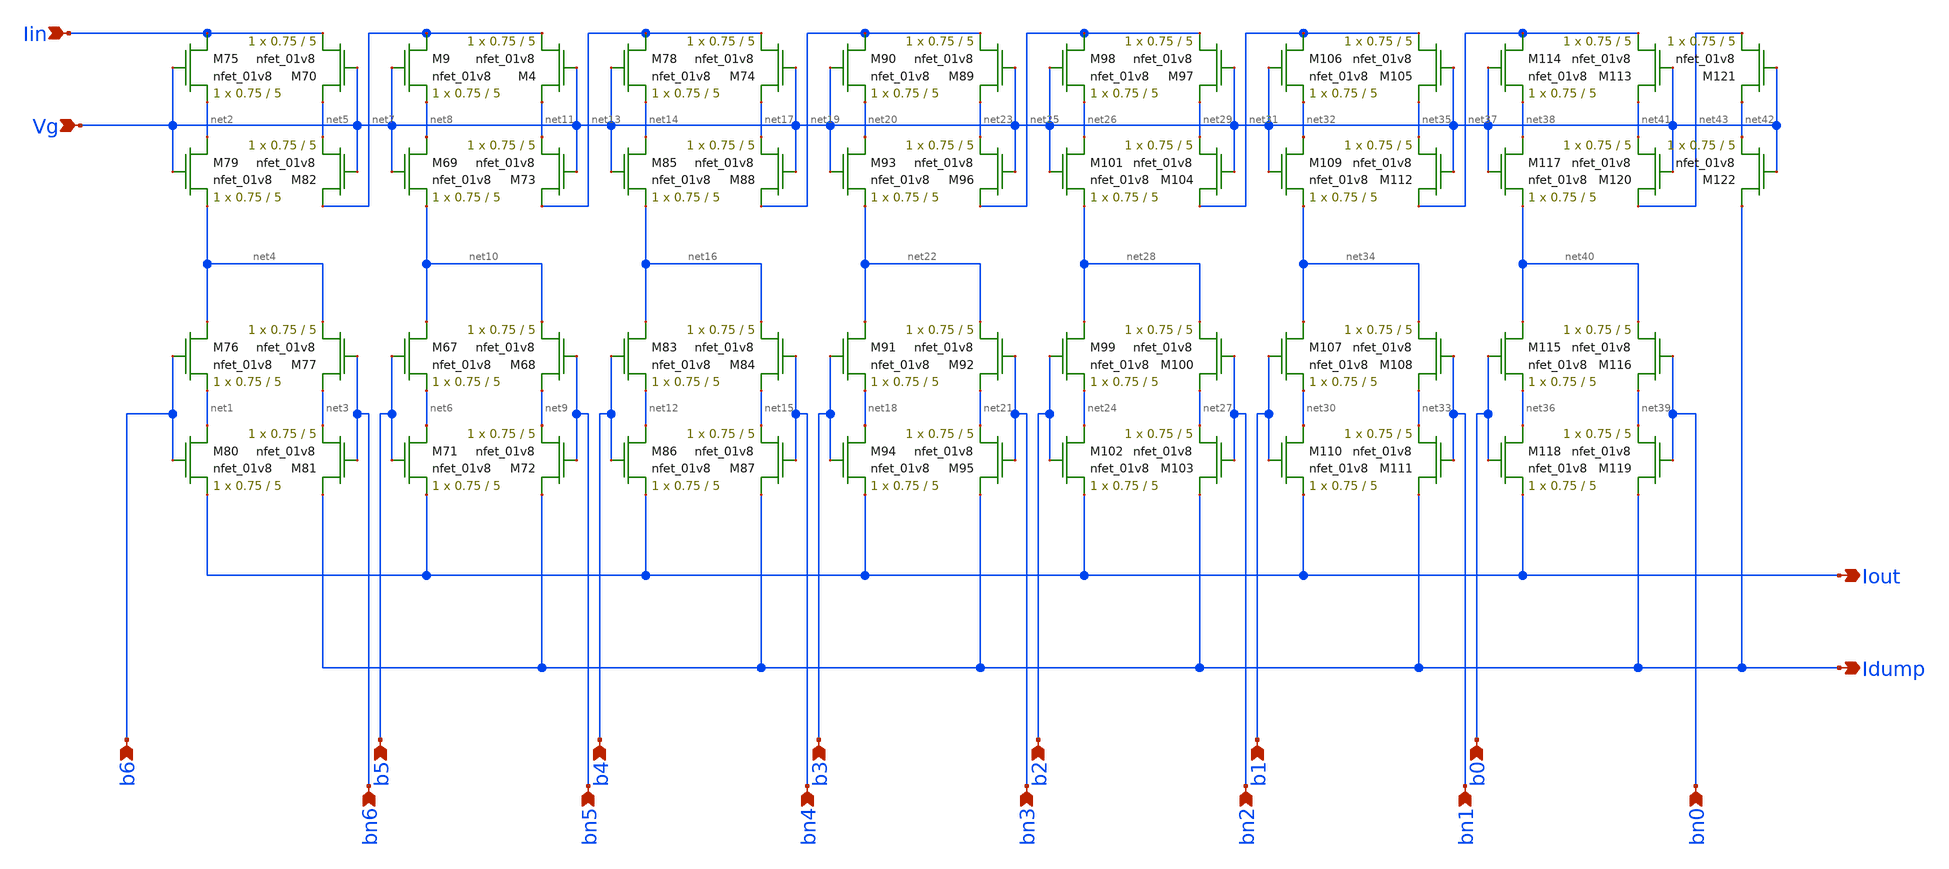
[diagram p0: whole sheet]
** sch_path: LDS_dac.sch
**.subckt LDS_dac Vg Iin Iout Idump b6 b5 b4 b3 b2 b1 b0 bn6 bn5 bn4 bn3 bn2 bn1 bn0
*.ipin Vg
*.ipin Iin
*.opin Iout
*.opin Idump
*.ipin b6
*.ipin b5
*.ipin b4
*.ipin b3
*.ipin b2
*.ipin b1
*.ipin b0
*.ipin bn6
*.ipin bn5
*.ipin bn4
*.ipin bn3
*.ipin bn2
*.ipin bn1
*.ipin bn0
XM70 net5 Vg Iin GND sky130_fd_pr__nfet_01v8 L=5 W=0.75 nf=1 ad='int((nf+1)/2) * W/nf * 0.29' as='int((nf+2)/2) * W/nf * 0.29'
+ pd='2*int((nf+1)/2) * (W/nf + 0.29)' ps='2*int((nf+2)/2) * (W/nf + 0.29)' nrd='0.29 / W' nrs='0.29 / W'
+ sa=0 sb=0 sd=0 mult=1 m=1
XM75 Iin Vg net2 GND sky130_fd_pr__nfet_01v8 L=5 W=0.75 nf=1 ad='int((nf+1)/2) * W/nf * 0.29' as='int((nf+2)/2) * W/nf * 0.29'
+ pd='2*int((nf+1)/2) * (W/nf + 0.29)' ps='2*int((nf+2)/2) * (W/nf + 0.29)' nrd='0.29 / W' nrs='0.29 / W'
+ sa=0 sb=0 sd=0 mult=1 m=1
XM76 net4 b6 net1 GND sky130_fd_pr__nfet_01v8 L=5 W=0.75 nf=1 ad='int((nf+1)/2) * W/nf * 0.29' as='int((nf+2)/2) * W/nf * 0.29'
+ pd='2*int((nf+1)/2) * (W/nf + 0.29)' ps='2*int((nf+2)/2) * (W/nf + 0.29)' nrd='0.29 / W' nrs='0.29 / W'
+ sa=0 sb=0 sd=0 mult=1 m=1
XM77 net3 bn6 net4 GND sky130_fd_pr__nfet_01v8 L=5 W=0.75 nf=1 ad='int((nf+1)/2) * W/nf * 0.29' as='int((nf+2)/2) * W/nf * 0.29'
+ pd='2*int((nf+1)/2) * (W/nf + 0.29)' ps='2*int((nf+2)/2) * (W/nf + 0.29)' nrd='0.29 / W' nrs='0.29 / W'
+ sa=0 sb=0 sd=0 mult=1 m=1
XM79 net2 Vg net4 GND sky130_fd_pr__nfet_01v8 L=5 W=0.75 nf=1 ad='int((nf+1)/2) * W/nf * 0.29' as='int((nf+2)/2) * W/nf * 0.29'
+ pd='2*int((nf+1)/2) * (W/nf + 0.29)' ps='2*int((nf+2)/2) * (W/nf + 0.29)' nrd='0.29 / W' nrs='0.29 / W'
+ sa=0 sb=0 sd=0 mult=1 m=1
XM80 net1 b6 Iout GND sky130_fd_pr__nfet_01v8 L=5 W=0.75 nf=1 ad='int((nf+1)/2) * W/nf * 0.29' as='int((nf+2)/2) * W/nf * 0.29'
+ pd='2*int((nf+1)/2) * (W/nf + 0.29)' ps='2*int((nf+2)/2) * (W/nf + 0.29)' nrd='0.29 / W' nrs='0.29 / W'
+ sa=0 sb=0 sd=0 mult=1 m=1
XM81 Idump bn6 net3 GND sky130_fd_pr__nfet_01v8 L=5 W=0.75 nf=1 ad='int((nf+1)/2) * W/nf * 0.29' as='int((nf+2)/2) * W/nf * 0.29'
+ pd='2*int((nf+1)/2) * (W/nf + 0.29)' ps='2*int((nf+2)/2) * (W/nf + 0.29)' nrd='0.29 / W' nrs='0.29 / W'
+ sa=0 sb=0 sd=0 mult=1 m=1
XM82 net7 Vg net5 GND sky130_fd_pr__nfet_01v8 L=5 W=0.75 nf=1 ad='int((nf+1)/2) * W/nf * 0.29' as='int((nf+2)/2) * W/nf * 0.29'
+ pd='2*int((nf+1)/2) * (W/nf + 0.29)' ps='2*int((nf+2)/2) * (W/nf + 0.29)' nrd='0.29 / W' nrs='0.29 / W'
+ sa=0 sb=0 sd=0 mult=1 m=1
XM4 net11 Vg net7 GND sky130_fd_pr__nfet_01v8 L=5 W=0.75 nf=1 ad='int((nf+1)/2) * W/nf * 0.29' as='int((nf+2)/2) * W/nf * 0.29'
+ pd='2*int((nf+1)/2) * (W/nf + 0.29)' ps='2*int((nf+2)/2) * (W/nf + 0.29)' nrd='0.29 / W' nrs='0.29 / W'
+ sa=0 sb=0 sd=0 mult=1 m=1
XM9 net7 Vg net8 GND sky130_fd_pr__nfet_01v8 L=5 W=0.75 nf=1 ad='int((nf+1)/2) * W/nf * 0.29' as='int((nf+2)/2) * W/nf * 0.29'
+ pd='2*int((nf+1)/2) * (W/nf + 0.29)' ps='2*int((nf+2)/2) * (W/nf + 0.29)' nrd='0.29 / W' nrs='0.29 / W'
+ sa=0 sb=0 sd=0 mult=1 m=1
XM67 net10 b5 net6 GND sky130_fd_pr__nfet_01v8 L=5 W=0.75 nf=1 ad='int((nf+1)/2) * W/nf * 0.29' as='int((nf+2)/2) * W/nf * 0.29'
+ pd='2*int((nf+1)/2) * (W/nf + 0.29)' ps='2*int((nf+2)/2) * (W/nf + 0.29)' nrd='0.29 / W' nrs='0.29 / W'
+ sa=0 sb=0 sd=0 mult=1 m=1
XM68 net9 bn5 net10 GND sky130_fd_pr__nfet_01v8 L=5 W=0.75 nf=1 ad='int((nf+1)/2) * W/nf * 0.29' as='int((nf+2)/2) * W/nf * 0.29'
+ pd='2*int((nf+1)/2) * (W/nf + 0.29)' ps='2*int((nf+2)/2) * (W/nf + 0.29)' nrd='0.29 / W' nrs='0.29 / W'
+ sa=0 sb=0 sd=0 mult=1 m=1
XM69 net8 Vg net10 GND sky130_fd_pr__nfet_01v8 L=5 W=0.75 nf=1 ad='int((nf+1)/2) * W/nf * 0.29' as='int((nf+2)/2) * W/nf * 0.29'
+ pd='2*int((nf+1)/2) * (W/nf + 0.29)' ps='2*int((nf+2)/2) * (W/nf + 0.29)' nrd='0.29 / W' nrs='0.29 / W'
+ sa=0 sb=0 sd=0 mult=1 m=1
XM71 net6 b5 Iout GND sky130_fd_pr__nfet_01v8 L=5 W=0.75 nf=1 ad='int((nf+1)/2) * W/nf * 0.29' as='int((nf+2)/2) * W/nf * 0.29'
+ pd='2*int((nf+1)/2) * (W/nf + 0.29)' ps='2*int((nf+2)/2) * (W/nf + 0.29)' nrd='0.29 / W' nrs='0.29 / W'
+ sa=0 sb=0 sd=0 mult=1 m=1
XM72 Idump bn5 net9 GND sky130_fd_pr__nfet_01v8 L=5 W=0.75 nf=1 ad='int((nf+1)/2) * W/nf * 0.29' as='int((nf+2)/2) * W/nf * 0.29'
+ pd='2*int((nf+1)/2) * (W/nf + 0.29)' ps='2*int((nf+2)/2) * (W/nf + 0.29)' nrd='0.29 / W' nrs='0.29 / W'
+ sa=0 sb=0 sd=0 mult=1 m=1
XM73 net13 Vg net11 GND sky130_fd_pr__nfet_01v8 L=5 W=0.75 nf=1 ad='int((nf+1)/2) * W/nf * 0.29' as='int((nf+2)/2) * W/nf * 0.29'
+ pd='2*int((nf+1)/2) * (W/nf + 0.29)' ps='2*int((nf+2)/2) * (W/nf + 0.29)' nrd='0.29 / W' nrs='0.29 / W'
+ sa=0 sb=0 sd=0 mult=1 m=1
XM74 net17 Vg net13 GND sky130_fd_pr__nfet_01v8 L=5 W=0.75 nf=1 ad='int((nf+1)/2) * W/nf * 0.29' as='int((nf+2)/2) * W/nf * 0.29'
+ pd='2*int((nf+1)/2) * (W/nf + 0.29)' ps='2*int((nf+2)/2) * (W/nf + 0.29)' nrd='0.29 / W' nrs='0.29 / W'
+ sa=0 sb=0 sd=0 mult=1 m=1
XM78 net13 Vg net14 GND sky130_fd_pr__nfet_01v8 L=5 W=0.75 nf=1 ad='int((nf+1)/2) * W/nf * 0.29' as='int((nf+2)/2) * W/nf * 0.29'
+ pd='2*int((nf+1)/2) * (W/nf + 0.29)' ps='2*int((nf+2)/2) * (W/nf + 0.29)' nrd='0.29 / W' nrs='0.29 / W'
+ sa=0 sb=0 sd=0 mult=1 m=1
XM83 net16 b4 net12 GND sky130_fd_pr__nfet_01v8 L=5 W=0.75 nf=1 ad='int((nf+1)/2) * W/nf * 0.29' as='int((nf+2)/2) * W/nf * 0.29'
+ pd='2*int((nf+1)/2) * (W/nf + 0.29)' ps='2*int((nf+2)/2) * (W/nf + 0.29)' nrd='0.29 / W' nrs='0.29 / W'
+ sa=0 sb=0 sd=0 mult=1 m=1
XM84 net15 bn4 net16 GND sky130_fd_pr__nfet_01v8 L=5 W=0.75 nf=1 ad='int((nf+1)/2) * W/nf * 0.29' as='int((nf+2)/2) * W/nf * 0.29'
+ pd='2*int((nf+1)/2) * (W/nf + 0.29)' ps='2*int((nf+2)/2) * (W/nf + 0.29)' nrd='0.29 / W' nrs='0.29 / W'
+ sa=0 sb=0 sd=0 mult=1 m=1
XM85 net14 Vg net16 GND sky130_fd_pr__nfet_01v8 L=5 W=0.75 nf=1 ad='int((nf+1)/2) * W/nf * 0.29' as='int((nf+2)/2) * W/nf * 0.29'
+ pd='2*int((nf+1)/2) * (W/nf + 0.29)' ps='2*int((nf+2)/2) * (W/nf + 0.29)' nrd='0.29 / W' nrs='0.29 / W'
+ sa=0 sb=0 sd=0 mult=1 m=1
XM86 net12 b4 Iout GND sky130_fd_pr__nfet_01v8 L=5 W=0.75 nf=1 ad='int((nf+1)/2) * W/nf * 0.29' as='int((nf+2)/2) * W/nf * 0.29'
+ pd='2*int((nf+1)/2) * (W/nf + 0.29)' ps='2*int((nf+2)/2) * (W/nf + 0.29)' nrd='0.29 / W' nrs='0.29 / W'
+ sa=0 sb=0 sd=0 mult=1 m=1
XM87 Idump bn4 net15 GND sky130_fd_pr__nfet_01v8 L=5 W=0.75 nf=1 ad='int((nf+1)/2) * W/nf * 0.29' as='int((nf+2)/2) * W/nf * 0.29'
+ pd='2*int((nf+1)/2) * (W/nf + 0.29)' ps='2*int((nf+2)/2) * (W/nf + 0.29)' nrd='0.29 / W' nrs='0.29 / W'
+ sa=0 sb=0 sd=0 mult=1 m=1
XM88 net19 Vg net17 GND sky130_fd_pr__nfet_01v8 L=5 W=0.75 nf=1 ad='int((nf+1)/2) * W/nf * 0.29' as='int((nf+2)/2) * W/nf * 0.29'
+ pd='2*int((nf+1)/2) * (W/nf + 0.29)' ps='2*int((nf+2)/2) * (W/nf + 0.29)' nrd='0.29 / W' nrs='0.29 / W'
+ sa=0 sb=0 sd=0 mult=1 m=1
XM89 net23 Vg net19 GND sky130_fd_pr__nfet_01v8 L=5 W=0.75 nf=1 ad='int((nf+1)/2) * W/nf * 0.29' as='int((nf+2)/2) * W/nf * 0.29'
+ pd='2*int((nf+1)/2) * (W/nf + 0.29)' ps='2*int((nf+2)/2) * (W/nf + 0.29)' nrd='0.29 / W' nrs='0.29 / W'
+ sa=0 sb=0 sd=0 mult=1 m=1
XM90 net19 Vg net20 GND sky130_fd_pr__nfet_01v8 L=5 W=0.75 nf=1 ad='int((nf+1)/2) * W/nf * 0.29' as='int((nf+2)/2) * W/nf * 0.29'
+ pd='2*int((nf+1)/2) * (W/nf + 0.29)' ps='2*int((nf+2)/2) * (W/nf + 0.29)' nrd='0.29 / W' nrs='0.29 / W'
+ sa=0 sb=0 sd=0 mult=1 m=1
XM91 net22 b3 net18 GND sky130_fd_pr__nfet_01v8 L=5 W=0.75 nf=1 ad='int((nf+1)/2) * W/nf * 0.29' as='int((nf+2)/2) * W/nf * 0.29'
+ pd='2*int((nf+1)/2) * (W/nf + 0.29)' ps='2*int((nf+2)/2) * (W/nf + 0.29)' nrd='0.29 / W' nrs='0.29 / W'
+ sa=0 sb=0 sd=0 mult=1 m=1
XM92 net21 bn3 net22 GND sky130_fd_pr__nfet_01v8 L=5 W=0.75 nf=1 ad='int((nf+1)/2) * W/nf * 0.29' as='int((nf+2)/2) * W/nf * 0.29'
+ pd='2*int((nf+1)/2) * (W/nf + 0.29)' ps='2*int((nf+2)/2) * (W/nf + 0.29)' nrd='0.29 / W' nrs='0.29 / W'
+ sa=0 sb=0 sd=0 mult=1 m=1
XM93 net20 Vg net22 GND sky130_fd_pr__nfet_01v8 L=5 W=0.75 nf=1 ad='int((nf+1)/2) * W/nf * 0.29' as='int((nf+2)/2) * W/nf * 0.29'
+ pd='2*int((nf+1)/2) * (W/nf + 0.29)' ps='2*int((nf+2)/2) * (W/nf + 0.29)' nrd='0.29 / W' nrs='0.29 / W'
+ sa=0 sb=0 sd=0 mult=1 m=1
XM94 net18 b3 Iout GND sky130_fd_pr__nfet_01v8 L=5 W=0.75 nf=1 ad='int((nf+1)/2) * W/nf * 0.29' as='int((nf+2)/2) * W/nf * 0.29'
+ pd='2*int((nf+1)/2) * (W/nf + 0.29)' ps='2*int((nf+2)/2) * (W/nf + 0.29)' nrd='0.29 / W' nrs='0.29 / W'
+ sa=0 sb=0 sd=0 mult=1 m=1
XM95 Idump bn3 net21 GND sky130_fd_pr__nfet_01v8 L=5 W=0.75 nf=1 ad='int((nf+1)/2) * W/nf * 0.29' as='int((nf+2)/2) * W/nf * 0.29'
+ pd='2*int((nf+1)/2) * (W/nf + 0.29)' ps='2*int((nf+2)/2) * (W/nf + 0.29)' nrd='0.29 / W' nrs='0.29 / W'
+ sa=0 sb=0 sd=0 mult=1 m=1
XM96 net25 Vg net23 GND sky130_fd_pr__nfet_01v8 L=5 W=0.75 nf=1 ad='int((nf+1)/2) * W/nf * 0.29' as='int((nf+2)/2) * W/nf * 0.29'
+ pd='2*int((nf+1)/2) * (W/nf + 0.29)' ps='2*int((nf+2)/2) * (W/nf + 0.29)' nrd='0.29 / W' nrs='0.29 / W'
+ sa=0 sb=0 sd=0 mult=1 m=1
XM97 net29 Vg net25 GND sky130_fd_pr__nfet_01v8 L=5 W=0.75 nf=1 ad='int((nf+1)/2) * W/nf * 0.29' as='int((nf+2)/2) * W/nf * 0.29'
+ pd='2*int((nf+1)/2) * (W/nf + 0.29)' ps='2*int((nf+2)/2) * (W/nf + 0.29)' nrd='0.29 / W' nrs='0.29 / W'
+ sa=0 sb=0 sd=0 mult=1 m=1
XM98 net25 Vg net26 GND sky130_fd_pr__nfet_01v8 L=5 W=0.75 nf=1 ad='int((nf+1)/2) * W/nf * 0.29' as='int((nf+2)/2) * W/nf * 0.29'
+ pd='2*int((nf+1)/2) * (W/nf + 0.29)' ps='2*int((nf+2)/2) * (W/nf + 0.29)' nrd='0.29 / W' nrs='0.29 / W'
+ sa=0 sb=0 sd=0 mult=1 m=1
XM99 net28 b2 net24 GND sky130_fd_pr__nfet_01v8 L=5 W=0.75 nf=1 ad='int((nf+1)/2) * W/nf * 0.29' as='int((nf+2)/2) * W/nf * 0.29'
+ pd='2*int((nf+1)/2) * (W/nf + 0.29)' ps='2*int((nf+2)/2) * (W/nf + 0.29)' nrd='0.29 / W' nrs='0.29 / W'
+ sa=0 sb=0 sd=0 mult=1 m=1
XM100 net27 bn2 net28 GND sky130_fd_pr__nfet_01v8 L=5 W=0.75 nf=1 ad='int((nf+1)/2) * W/nf * 0.29' as='int((nf+2)/2) * W/nf * 0.29'
+ pd='2*int((nf+1)/2) * (W/nf + 0.29)' ps='2*int((nf+2)/2) * (W/nf + 0.29)' nrd='0.29 / W' nrs='0.29 / W'
+ sa=0 sb=0 sd=0 mult=1 m=1
XM101 net26 Vg net28 GND sky130_fd_pr__nfet_01v8 L=5 W=0.75 nf=1 ad='int((nf+1)/2) * W/nf * 0.29' as='int((nf+2)/2) * W/nf * 0.29'
+ pd='2*int((nf+1)/2) * (W/nf + 0.29)' ps='2*int((nf+2)/2) * (W/nf + 0.29)' nrd='0.29 / W' nrs='0.29 / W'
+ sa=0 sb=0 sd=0 mult=1 m=1
XM102 net24 b2 Iout GND sky130_fd_pr__nfet_01v8 L=5 W=0.75 nf=1 ad='int((nf+1)/2) * W/nf * 0.29' as='int((nf+2)/2) * W/nf * 0.29'
+ pd='2*int((nf+1)/2) * (W/nf + 0.29)' ps='2*int((nf+2)/2) * (W/nf + 0.29)' nrd='0.29 / W' nrs='0.29 / W'
+ sa=0 sb=0 sd=0 mult=1 m=1
XM103 Idump bn2 net27 GND sky130_fd_pr__nfet_01v8 L=5 W=0.75 nf=1 ad='int((nf+1)/2) * W/nf * 0.29' as='int((nf+2)/2) * W/nf * 0.29'
+ pd='2*int((nf+1)/2) * (W/nf + 0.29)' ps='2*int((nf+2)/2) * (W/nf + 0.29)' nrd='0.29 / W' nrs='0.29 / W'
+ sa=0 sb=0 sd=0 mult=1 m=1
XM104 net31 Vg net29 GND sky130_fd_pr__nfet_01v8 L=5 W=0.75 nf=1 ad='int((nf+1)/2) * W/nf * 0.29' as='int((nf+2)/2) * W/nf * 0.29'
+ pd='2*int((nf+1)/2) * (W/nf + 0.29)' ps='2*int((nf+2)/2) * (W/nf + 0.29)' nrd='0.29 / W' nrs='0.29 / W'
+ sa=0 sb=0 sd=0 mult=1 m=1
XM105 net35 Vg net31 GND sky130_fd_pr__nfet_01v8 L=5 W=0.75 nf=1 ad='int((nf+1)/2) * W/nf * 0.29' as='int((nf+2)/2) * W/nf * 0.29'
+ pd='2*int((nf+1)/2) * (W/nf + 0.29)' ps='2*int((nf+2)/2) * (W/nf + 0.29)' nrd='0.29 / W' nrs='0.29 / W'
+ sa=0 sb=0 sd=0 mult=1 m=1
XM106 net31 Vg net32 GND sky130_fd_pr__nfet_01v8 L=5 W=0.75 nf=1 ad='int((nf+1)/2) * W/nf * 0.29' as='int((nf+2)/2) * W/nf * 0.29'
+ pd='2*int((nf+1)/2) * (W/nf + 0.29)' ps='2*int((nf+2)/2) * (W/nf + 0.29)' nrd='0.29 / W' nrs='0.29 / W'
+ sa=0 sb=0 sd=0 mult=1 m=1
XM107 net34 b1 net30 GND sky130_fd_pr__nfet_01v8 L=5 W=0.75 nf=1 ad='int((nf+1)/2) * W/nf * 0.29' as='int((nf+2)/2) * W/nf * 0.29'
+ pd='2*int((nf+1)/2) * (W/nf + 0.29)' ps='2*int((nf+2)/2) * (W/nf + 0.29)' nrd='0.29 / W' nrs='0.29 / W'
+ sa=0 sb=0 sd=0 mult=1 m=1
XM108 net33 bn1 net34 GND sky130_fd_pr__nfet_01v8 L=5 W=0.75 nf=1 ad='int((nf+1)/2) * W/nf * 0.29' as='int((nf+2)/2) * W/nf * 0.29'
+ pd='2*int((nf+1)/2) * (W/nf + 0.29)' ps='2*int((nf+2)/2) * (W/nf + 0.29)' nrd='0.29 / W' nrs='0.29 / W'
+ sa=0 sb=0 sd=0 mult=1 m=1
XM109 net32 Vg net34 GND sky130_fd_pr__nfet_01v8 L=5 W=0.75 nf=1 ad='int((nf+1)/2) * W/nf * 0.29' as='int((nf+2)/2) * W/nf * 0.29'
+ pd='2*int((nf+1)/2) * (W/nf + 0.29)' ps='2*int((nf+2)/2) * (W/nf + 0.29)' nrd='0.29 / W' nrs='0.29 / W'
+ sa=0 sb=0 sd=0 mult=1 m=1
XM110 net30 b1 Iout GND sky130_fd_pr__nfet_01v8 L=5 W=0.75 nf=1 ad='int((nf+1)/2) * W/nf * 0.29' as='int((nf+2)/2) * W/nf * 0.29'
+ pd='2*int((nf+1)/2) * (W/nf + 0.29)' ps='2*int((nf+2)/2) * (W/nf + 0.29)' nrd='0.29 / W' nrs='0.29 / W'
+ sa=0 sb=0 sd=0 mult=1 m=1
XM111 Idump bn1 net33 GND sky130_fd_pr__nfet_01v8 L=5 W=0.75 nf=1 ad='int((nf+1)/2) * W/nf * 0.29' as='int((nf+2)/2) * W/nf * 0.29'
+ pd='2*int((nf+1)/2) * (W/nf + 0.29)' ps='2*int((nf+2)/2) * (W/nf + 0.29)' nrd='0.29 / W' nrs='0.29 / W'
+ sa=0 sb=0 sd=0 mult=1 m=1
XM112 net37 Vg net35 GND sky130_fd_pr__nfet_01v8 L=5 W=0.75 nf=1 ad='int((nf+1)/2) * W/nf * 0.29' as='int((nf+2)/2) * W/nf * 0.29'
+ pd='2*int((nf+1)/2) * (W/nf + 0.29)' ps='2*int((nf+2)/2) * (W/nf + 0.29)' nrd='0.29 / W' nrs='0.29 / W'
+ sa=0 sb=0 sd=0 mult=1 m=1
XM113 net41 Vg net37 GND sky130_fd_pr__nfet_01v8 L=5 W=0.75 nf=1 ad='int((nf+1)/2) * W/nf * 0.29' as='int((nf+2)/2) * W/nf * 0.29'
+ pd='2*int((nf+1)/2) * (W/nf + 0.29)' ps='2*int((nf+2)/2) * (W/nf + 0.29)' nrd='0.29 / W' nrs='0.29 / W'
+ sa=0 sb=0 sd=0 mult=1 m=1
XM114 net37 Vg net38 GND sky130_fd_pr__nfet_01v8 L=5 W=0.75 nf=1 ad='int((nf+1)/2) * W/nf * 0.29' as='int((nf+2)/2) * W/nf * 0.29'
+ pd='2*int((nf+1)/2) * (W/nf + 0.29)' ps='2*int((nf+2)/2) * (W/nf + 0.29)' nrd='0.29 / W' nrs='0.29 / W'
+ sa=0 sb=0 sd=0 mult=1 m=1
XM115 net40 b0 net36 GND sky130_fd_pr__nfet_01v8 L=5 W=0.75 nf=1 ad='int((nf+1)/2) * W/nf * 0.29' as='int((nf+2)/2) * W/nf * 0.29'
+ pd='2*int((nf+1)/2) * (W/nf + 0.29)' ps='2*int((nf+2)/2) * (W/nf + 0.29)' nrd='0.29 / W' nrs='0.29 / W'
+ sa=0 sb=0 sd=0 mult=1 m=1
XM116 net39 bn0 net40 GND sky130_fd_pr__nfet_01v8 L=5 W=0.75 nf=1 ad='int((nf+1)/2) * W/nf * 0.29' as='int((nf+2)/2) * W/nf * 0.29'
+ pd='2*int((nf+1)/2) * (W/nf + 0.29)' ps='2*int((nf+2)/2) * (W/nf + 0.29)' nrd='0.29 / W' nrs='0.29 / W'
+ sa=0 sb=0 sd=0 mult=1 m=1
XM117 net38 Vg net40 GND sky130_fd_pr__nfet_01v8 L=5 W=0.75 nf=1 ad='int((nf+1)/2) * W/nf * 0.29' as='int((nf+2)/2) * W/nf * 0.29'
+ pd='2*int((nf+1)/2) * (W/nf + 0.29)' ps='2*int((nf+2)/2) * (W/nf + 0.29)' nrd='0.29 / W' nrs='0.29 / W'
+ sa=0 sb=0 sd=0 mult=1 m=1
XM118 net36 b0 Iout GND sky130_fd_pr__nfet_01v8 L=5 W=0.75 nf=1 ad='int((nf+1)/2) * W/nf * 0.29' as='int((nf+2)/2) * W/nf * 0.29'
+ pd='2*int((nf+1)/2) * (W/nf + 0.29)' ps='2*int((nf+2)/2) * (W/nf + 0.29)' nrd='0.29 / W' nrs='0.29 / W'
+ sa=0 sb=0 sd=0 mult=1 m=1
XM119 Idump bn0 net39 GND sky130_fd_pr__nfet_01v8 L=5 W=0.75 nf=1 ad='int((nf+1)/2) * W/nf * 0.29' as='int((nf+2)/2) * W/nf * 0.29'
+ pd='2*int((nf+1)/2) * (W/nf + 0.29)' ps='2*int((nf+2)/2) * (W/nf + 0.29)' nrd='0.29 / W' nrs='0.29 / W'
+ sa=0 sb=0 sd=0 mult=1 m=1
XM120 net43 Vg net41 GND sky130_fd_pr__nfet_01v8 L=5 W=0.75 nf=1 ad='int((nf+1)/2) * W/nf * 0.29' as='int((nf+2)/2) * W/nf * 0.29'
+ pd='2*int((nf+1)/2) * (W/nf + 0.29)' ps='2*int((nf+2)/2) * (W/nf + 0.29)' nrd='0.29 / W' nrs='0.29 / W'
+ sa=0 sb=0 sd=0 mult=1 m=1
XM121 net42 Vg net43 GND sky130_fd_pr__nfet_01v8 L=5 W=0.75 nf=1 ad='int((nf+1)/2) * W/nf * 0.29' as='int((nf+2)/2) * W/nf * 0.29'
+ pd='2*int((nf+1)/2) * (W/nf + 0.29)' ps='2*int((nf+2)/2) * (W/nf + 0.29)' nrd='0.29 / W' nrs='0.29 / W'
+ sa=0 sb=0 sd=0 mult=1 m=1
XM122 Idump Vg net42 GND sky130_fd_pr__nfet_01v8 L=5 W=0.75 nf=1 ad='int((nf+1)/2) * W/nf * 0.29' as='int((nf+2)/2) * W/nf * 0.29'
+ pd='2*int((nf+1)/2) * (W/nf + 0.29)' ps='2*int((nf+2)/2) * (W/nf + 0.29)' nrd='0.29 / W' nrs='0.29 / W'
+ sa=0 sb=0 sd=0 mult=1 m=1
**.ends
.end
